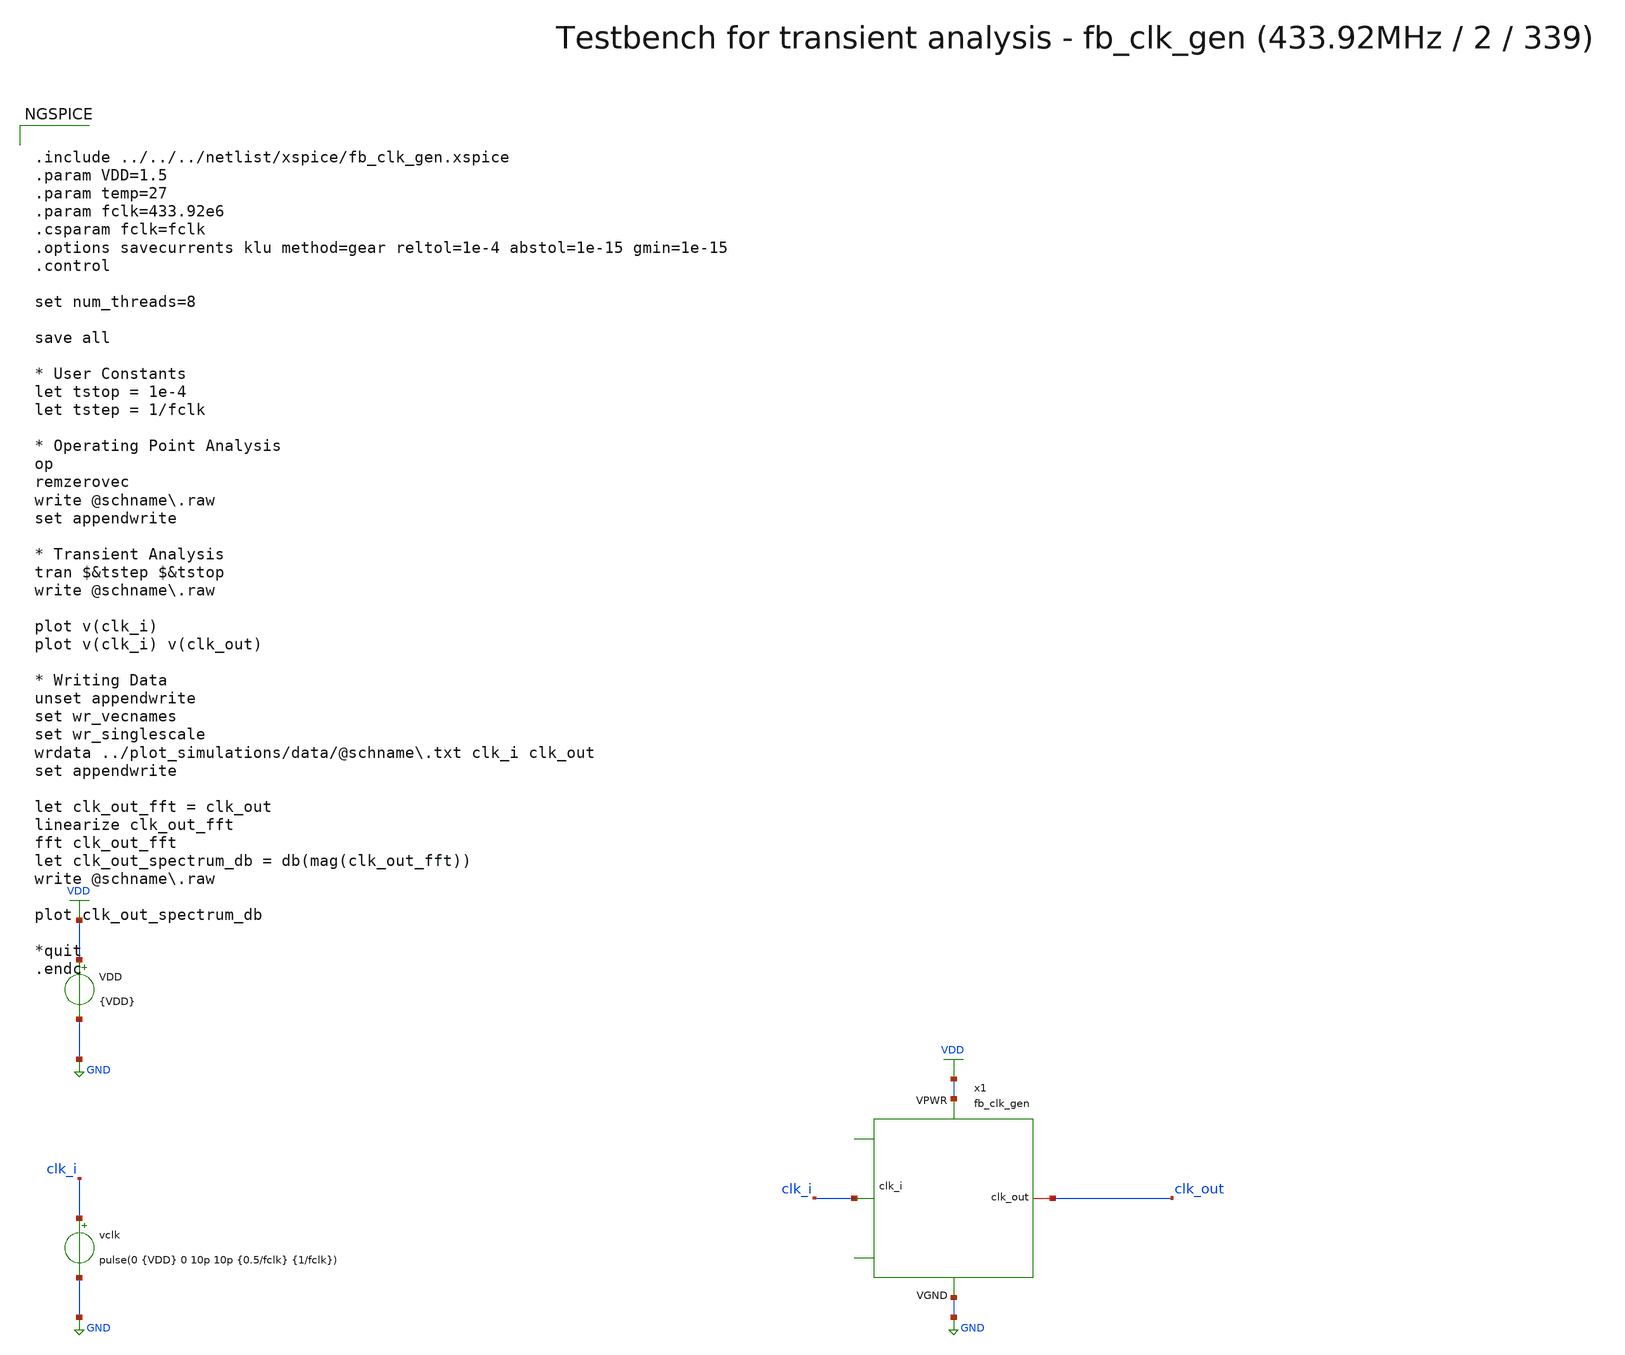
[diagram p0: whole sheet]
** sch_path: macros/heichips26_ook/macros/fb_clk_gen/testbenches/xschem/fb_clk_gen_tb_tran.sch
**.subckt fb_clk_gen_tb_tran
VDD VDD GND {VDD}
vclk clk_i GND pulse(0 {VDD} 0 10p 10p {0.5/fclk} {1/fclk})
x1 VDD GND clk_i clk_out fb_clk_gen
**** begin user architecture code


.include ../../../netlist/xspice/fb_clk_gen.xspice
.param VDD=1.5
.param temp=27
.param fclk=433.92e6
.csparam fclk=fclk
.options savecurrents klu method=gear reltol=1e-4 abstol=1e-15 gmin=1e-15
.control

set num_threads=8

save all

* User Constants
let tstop = 1e-4
let tstep = 1/fclk

* Operating Point Analysis
op
remzerovec
write @schname\.raw
set appendwrite

* Transient Analysis
tran $&tstep $&tstop
write @schname\.raw

plot v(clk_i)
plot v(clk_i) v(clk_out)

* Writing Data
unset appendwrite
set wr_vecnames
set wr_singlescale
wrdata ../plot_simulations/data/@schname\.txt clk_i clk_out
set appendwrite

let clk_out_fft = clk_out
linearize clk_out_fft
fft clk_out_fft
let clk_out_spectrum_db = db(mag(clk_out_fft))
write @schname\.raw

plot clk_out_spectrum_db

*quit
.endc


.lib cornerMOSlv.lib mos_tt
.lib cornerMOShv.lib mos_tt
.lib cornerRES.lib res_typ
.lib cornerDIO.lib dio_tt

**** end user architecture code
**.ends
.GLOBAL GND
.GLOBAL VDD
.end
